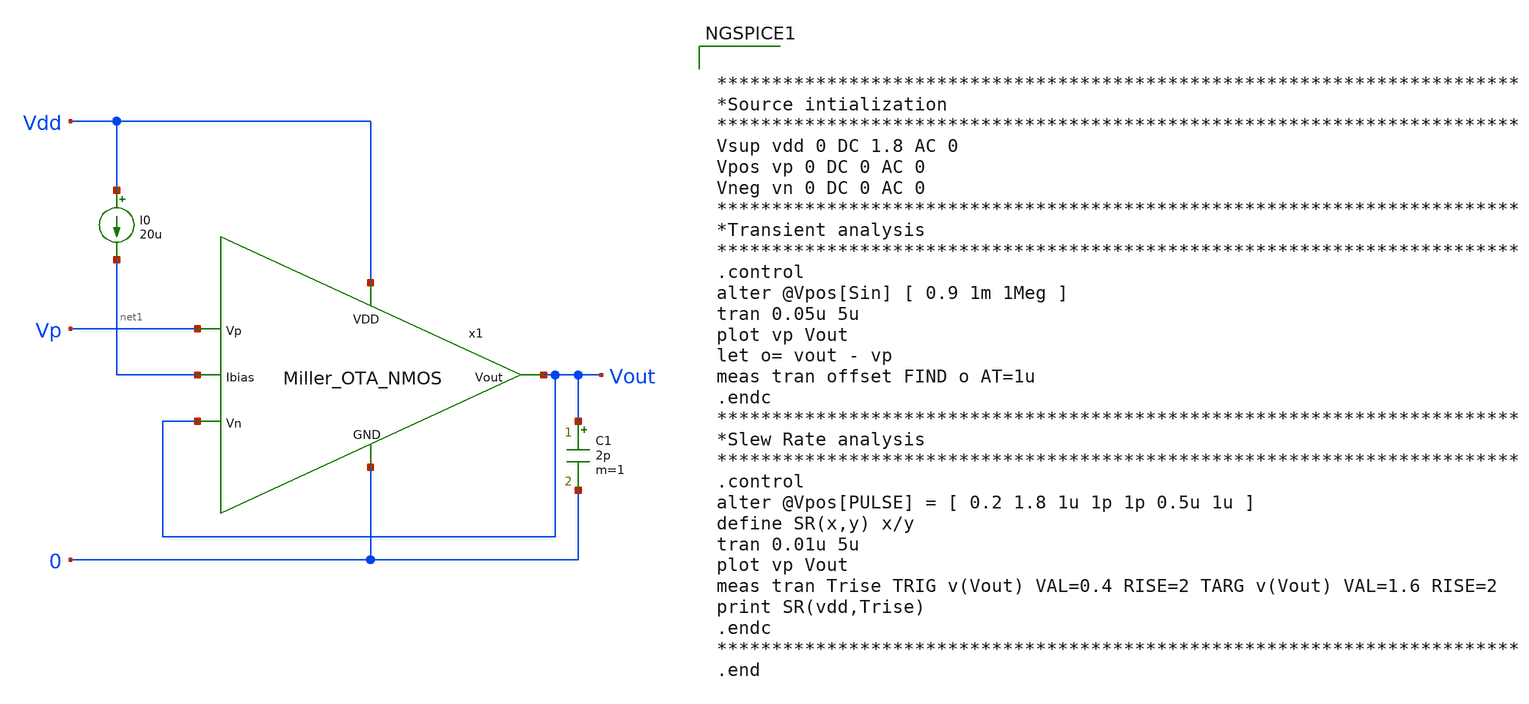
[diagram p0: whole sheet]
** sch_path: Analog_blocks/Analog_Blocks/OTA/Testbench/Miller_OTA/Transistor5v/Miller_OTA5v_meas_transient.sch
**.subckt Miller_OTA5v_meas_transient
I0 Vdd net1 20u
C1 Vout 0 2p m=1
x1 Vdd Vout Vp Vout net1 0 Miller_OTA_NMOS
**** begin user architecture code


*************************************************************************
*Source intialization
*************************************************************************
Vsup vdd 0 DC 1.8 AC 0
Vpos vp 0 DC 0 AC 0
Vneg vn 0 DC 0 AC 0
*************************************************************************
*Transient analysis
*************************************************************************
.control
alter @Vpos[Sin] [ 0.9 1m 1Meg ]
tran 0.05u 5u
plot vp Vout
let o= vout - vp
meas tran offset FIND o AT=1u
.endc
*************************************************************************
*Slew Rate analysis
*************************************************************************
.control
alter @Vpos[PULSE] = [ 0.2 1.8 1u 1p 1p 0.5u 1u ]
define SR(x,y) x/y
tran 0.01u 5u
plot vp Vout
meas tran Trise TRIG v(Vout) VAL=0.4 RISE=2 TARG v(Vout) VAL=1.6 RISE=2
print SR(vdd,Trise)
.endc
*************************************************************************
.end




.param mc_mm_switch=0
.param mc_pr_switch=0
.include ~/mabrains/Analog_blocks/models/sky130A/libs.ref/sky130_fd_pr/spice/sky130_fd_pr__nfet_01v8__tt.corner.spice
.include ~/mabrains/Analog_blocks/models/sky130A/libs.ref/sky130_fd_pr/spice/sky130_fd_pr__nfet_01v8_lvt__tt.corner.spice
.include ~/mabrains/Analog_blocks/models/sky130A/libs.ref/sky130_fd_pr/spice/sky130_fd_pr__pfet_01v8__tt.corner.spice
.include ~/mabrains/Analog_blocks/models/sky130A/libs.ref/sky130_fd_pr/spice/sky130_fd_pr__nfet_03v3_nvt__tt.corner.spice
.include ~/mabrains/Analog_blocks/models/sky130A/libs.ref/sky130_fd_pr/spice/sky130_fd_pr__nfet_05v0_nvt__tt.corner.spice
.include ~/mabrains/Analog_blocks/models/sky130A/libs.ref/sky130_fd_pr/spice/sky130_fd_pr__esd_nfet_01v8__tt.corner.spice
.include ~/mabrains/Analog_blocks/models/sky130A/libs.ref/sky130_fd_pr/spice/sky130_fd_pr__pfet_01v8_lvt__tt.corner.spice
.include ~/mabrains/Analog_blocks/models/sky130A/libs.ref/sky130_fd_pr/spice/sky130_fd_pr__pfet_01v8_hvt__tt.corner.spice
.include ~/mabrains/Analog_blocks/models/sky130A/libs.ref/sky130_fd_pr/spice/sky130_fd_pr__esd_pfet_g5v0d10v5__tt.corner.spice
.include ~/mabrains/Analog_blocks/models/sky130A/libs.ref/sky130_fd_pr/spice/sky130_fd_pr__pfet_g5v0d10v5__tt.corner.spice
.include ~/mabrains/Analog_blocks/models/sky130A/libs.ref/sky130_fd_pr/spice/sky130_fd_pr__pfet_g5v0d16v0__tt.corner.spice
.include ~/mabrains/Analog_blocks/models/sky130A/libs.ref/sky130_fd_pr/spice/sky130_fd_pr__nfet_g5v0d10v5__tt.corner.spice
.include ~/mabrains/Analog_blocks/models/sky130A/libs.ref/sky130_fd_pr/spice/sky130_fd_pr__nfet_g5v0d16v0__tt_discrete.corner.spice
.include ~/mabrains/Analog_blocks/models/sky130A/libs.ref/sky130_fd_pr/spice/sky130_fd_pr__esd_nfet_g5v0d10v5__tt.corner.spice
.include ~/mabrains/Analog_blocks/models/sky130A/libs.ref/sky130_fd_pr/spice/sky130_fd_pr__nfet_20v0__tt_discrete.corner.spice
.include ~/mabrains/Analog_blocks/models/sky130A/libs.ref/sky130_fd_pr/spice/sky130_fd_pr__pfet_20v0__tt_discrete.corner.spice
.include ~/mabrains/Analog_blocks/models/sky130A/libs.tech/ngspice/corners/tt/nonfet.spice
* Mismatch parameters
.include ~/mabrains/Analog_blocks/models/sky130A/libs.ref/sky130_fd_pr/spice/sky130_fd_pr__nfet_01v8__mismatch.corner.spice
.include ~/mabrains/Analog_blocks/models/sky130A/libs.ref/sky130_fd_pr/spice/sky130_fd_pr__pfet_01v8__mismatch.corner.spice
.include ~/mabrains/Analog_blocks/models/sky130A/libs.ref/sky130_fd_pr/spice/sky130_fd_pr__nfet_01v8_lvt__mismatch.corner.spice
.include ~/mabrains/Analog_blocks/models/sky130A/libs.ref/sky130_fd_pr/spice/sky130_fd_pr__pfet_01v8_lvt__mismatch.corner.spice
.include ~/mabrains/Analog_blocks/models/sky130A/libs.ref/sky130_fd_pr/spice/sky130_fd_pr__pfet_01v8_hvt__mismatch.corner.spice
.include ~/mabrains/Analog_blocks/models/sky130A/libs.ref/sky130_fd_pr/spice/sky130_fd_pr__nfet_g5v0d10v5__mismatch.corner.spice
.include ~/mabrains/Analog_blocks/models/sky130A/libs.ref/sky130_fd_pr/spice/sky130_fd_pr__pfet_g5v0d10v5__mismatch.corner.spice
.include ~/mabrains/Analog_blocks/models/sky130A/libs.ref/sky130_fd_pr/spice/sky130_fd_pr__nfet_05v0_nvt__mismatch.corner.spice
.include ~/mabrains/Analog_blocks/models/sky130A/libs.ref/sky130_fd_pr/spice/sky130_fd_pr__nfet_03v3_nvt__mismatch.corner.spice
* Resistor/Capacitor
.include ~/mabrains/Analog_blocks/models/sky130A/libs.tech/ngspice/r+c/res_typical__cap_typical.spice
.include ~/mabrains/Analog_blocks/models/sky130A/libs.tech/ngspice/r+c/res_typical__cap_typical__lin.spice
* Special cells
.include ~/mabrains/Analog_blocks/models/sky130A/libs.tech/ngspice/corners/tt/specialized_cells.spice
* All models
.include ~/mabrains/Analog_blocks/models/sky130A/libs.tech/ngspice/all.spice
* Corner
.include ~/mabrains/Analog_blocks/models/sky130A/libs.tech/ngspice/corners/tt/rf.spice



**** end user architecture code
**.ends

* expanding   symbol:
*+  /home/eslam/mabrains/Analog_blocks/Analog_Blocks/OTA/Schematic/Miller_OTA/Transistor5v/Miller_OTA_NMOS.sym # of pins=6
** sym_path: Analog_Blocks/OTA/Schematic/Miller_OTA/Transistor5v/Miller_OTA_NMOS.sym
** sch_path: Analog_Blocks/OTA/Schematic/Miller_OTA/Transistor5v/Miller_OTA_NMOS.sch
.subckt Miller_OTA_NMOS VDD Vn Vp Vout Ibias GND
*.ipin VDD
*.ipin Ibias
*.ipin Vn
*.ipin Vp
*.opin Vout
*.ipin GND
XM1 net1 Vn net3 GND sky130_fd_pr__nfet_g5v0d10v5 L=0.5 W=10 nf=1 ad='int((nf+1)/2) * W/nf * 0.29' as='int((nf+2)/2) * W/nf * 0.29'
+ pd='2*int((nf+1)/2) * (W/nf + 0.29)' ps='2*int((nf+2)/2) * (W/nf + 0.29)' nrd='0.29 / W' nrs='0.29 / W'
+ sa=0 sb=0 sd=0 mult=8 m=8
XM2 net2 Vp net3 GND sky130_fd_pr__nfet_g5v0d10v5 L=0.5 W=10 nf=1 ad='int((nf+1)/2) * W/nf * 0.29' as='int((nf+2)/2) * W/nf * 0.29'
+ pd='2*int((nf+1)/2) * (W/nf + 0.29)' ps='2*int((nf+2)/2) * (W/nf + 0.29)' nrd='0.29 / W' nrs='0.29 / W'
+ sa=0 sb=0 sd=0 mult=8 m=8
XM3 net1 net1 VDD VDD sky130_fd_pr__pfet_g5v0d10v5 L=0.5 W=5 nf=1 ad='int((nf+1)/2) * W/nf * 0.29' as='int((nf+2)/2) * W/nf * 0.29'
+ pd='2*int((nf+1)/2) * (W/nf + 0.29)' ps='2*int((nf+2)/2) * (W/nf + 0.29)' nrd='0.29 / W' nrs='0.29 / W'
+ sa=0 sb=0 sd=0 mult=4 m=4
XM4 net2 net1 VDD VDD sky130_fd_pr__pfet_g5v0d10v5 L=0.5 W=5 nf=1 ad='int((nf+1)/2) * W/nf * 0.29' as='int((nf+2)/2) * W/nf * 0.29'
+ pd='2*int((nf+1)/2) * (W/nf + 0.29)' ps='2*int((nf+2)/2) * (W/nf + 0.29)' nrd='0.29 / W' nrs='0.29 / W'
+ sa=0 sb=0 sd=0 mult=4 m=4
XM6 Vout net2 VDD VDD sky130_fd_pr__pfet_g5v0d10v5 L=0.5 W=5 nf=1 ad='int((nf+1)/2) * W/nf * 0.29' as='int((nf+2)/2) * W/nf * 0.29'
+ pd='2*int((nf+1)/2) * (W/nf + 0.29)' ps='2*int((nf+2)/2) * (W/nf + 0.29)' nrd='0.29 / W' nrs='0.29 / W'
+ sa=0 sb=0 sd=0 mult=20 m=20
XM5 net3 Ibias GND GND sky130_fd_pr__nfet_g5v0d10v5 L=1 W=3 nf=1 ad='int((nf+1)/2) * W/nf * 0.29' as='int((nf+2)/2) * W/nf * 0.29'
+ pd='2*int((nf+1)/2) * (W/nf + 0.29)' ps='2*int((nf+2)/2) * (W/nf + 0.29)' nrd='0.29 / W' nrs='0.29 / W'
+ sa=0 sb=0 sd=0 mult=8 m=8
XM8 Ibias Ibias GND GND sky130_fd_pr__nfet_g5v0d10v5 L=1 W=3 nf=1 ad='int((nf+1)/2) * W/nf * 0.29' as='int((nf+2)/2) * W/nf * 0.29'
+ pd='2*int((nf+1)/2) * (W/nf + 0.29)' ps='2*int((nf+2)/2) * (W/nf + 0.29)' nrd='0.29 / W' nrs='0.29 / W'
+ sa=0 sb=0 sd=0 mult=8 m=8
XC1 net2 Vout sky130_fd_pr__cap_mim_m3_2 W=25 L=25 MF=1 m=1
XM7 Vout Ibias GND GND sky130_fd_pr__nfet_g5v0d10v5 L=1 W=3 nf=1 ad='int((nf+1)/2) * W/nf * 0.29' as='int((nf+2)/2) * W/nf * 0.29'
+ pd='2*int((nf+1)/2) * (W/nf + 0.29)' ps='2*int((nf+2)/2) * (W/nf + 0.29)' nrd='0.29 / W' nrs='0.29 / W'
+ sa=0 sb=0 sd=0 mult=16 m=16
.ends

.end
